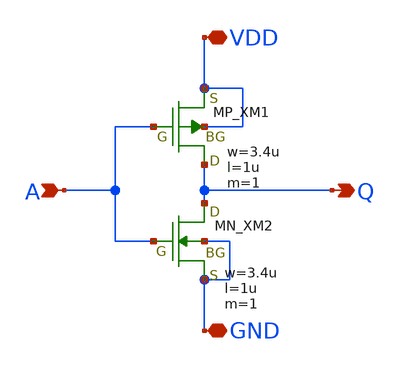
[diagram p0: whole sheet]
** sch_path: inverter/inverter_xu_wenying.sch
**.subckt inverter_xu_wenying VDD A Q GND
*.iopin VDD
*.ipin A
*.opin Q
*.iopin GND
XXM1 Q A VDD VDD PMOS w=3.4u l=1u nrd=0 nrs=0 m=1
XXM2 Q A GND GND NMOS w=3.4u l=1u nrd=0 nrs=0 m=1
**.ends
.end
